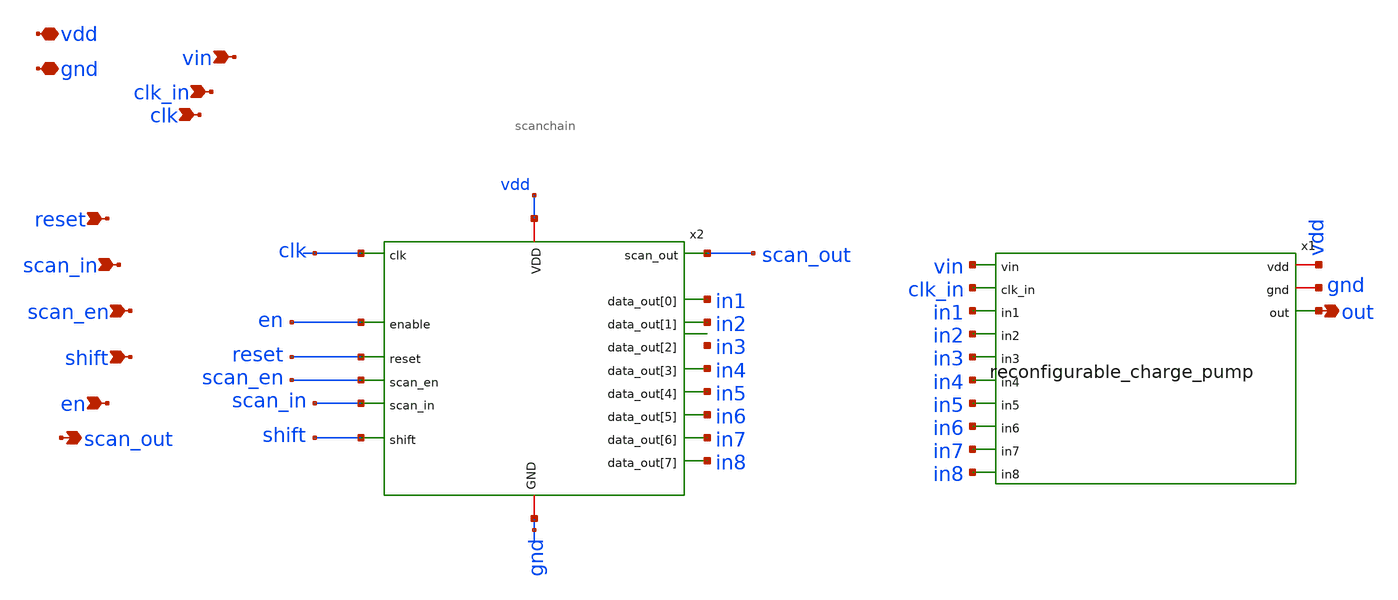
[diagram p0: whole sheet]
** sch_path: xschem/reconfigurable_CP_withScanchain2.sch
**.subckt reconfigurable_CP_withScanchain2 gnd vdd vin clk_in clk reset scan_in scan_en shift en out
*+ scan_out
*.iopin gnd
*.iopin vdd
*.ipin vin
*.ipin clk_in
*.ipin clk
*.ipin reset
*.ipin scan_in
*.ipin scan_en
*.ipin shift
*.ipin en
*.opin out
*.opin scan_out
x2 clk in3 in6 in8 en reset scan_en scan_in scan_out shift in5 in2 in7 in4 vdd gnd in1 scanchain
x1 vin clk_in vdd gnd in1 in2 in3 in4 in5 in6 in7 in8 out reconfigurable_charge_pump
**.ends
.end
